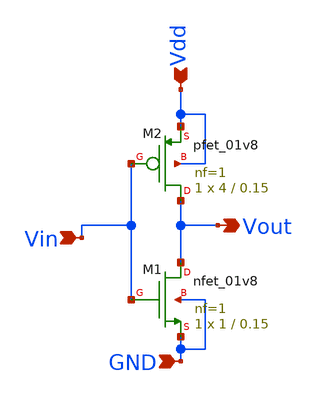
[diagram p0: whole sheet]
** sch_path: xschem/inv_vtc.sch
**.subckt inv_vtc Vin Vdd GND Vout
*.ipin Vin
*.ipin Vdd
*.ipin GND
*.opin Vout
XM1 Vout Vin GND GND sky130_fd_pr__nfet_01v8 L=0.15 W=1 nf=1 ad='int((1 + 1)/2) * 1 / 1 * 0.29' as='int((1 + 2)/2) * 1 / 1 * 0.29'
+ pd='2*int((1 + 1)/2) * (1 / 1 + 0.29)' ps='2*int((1 + 2)/2) * (1 / 1 + 0.29)' nrd='0.29 / 1 ' nrs='0.29 / 1 '
+ sa=0 sb=0 sd=0 mult=1 m=1
XM2 Vout Vin Vdd Vdd sky130_fd_pr__pfet_01v8 L=0.15 W=4 nf=1 ad='int((1 + 1)/2) * 4 / 1 * 0.29' as='int((1 + 2)/2) * 4 / 1 * 0.29'
+ pd='2*int((1 + 1)/2) * (4 / 1 + 0.29)' ps='2*int((1 + 2)/2) * (4 / 1 + 0.29)' nrd='0.29 / 4 ' nrs='0.29 / 4 '
+ sa=0 sb=0 sd=0 mult=1 m=1
**.ends
.end
